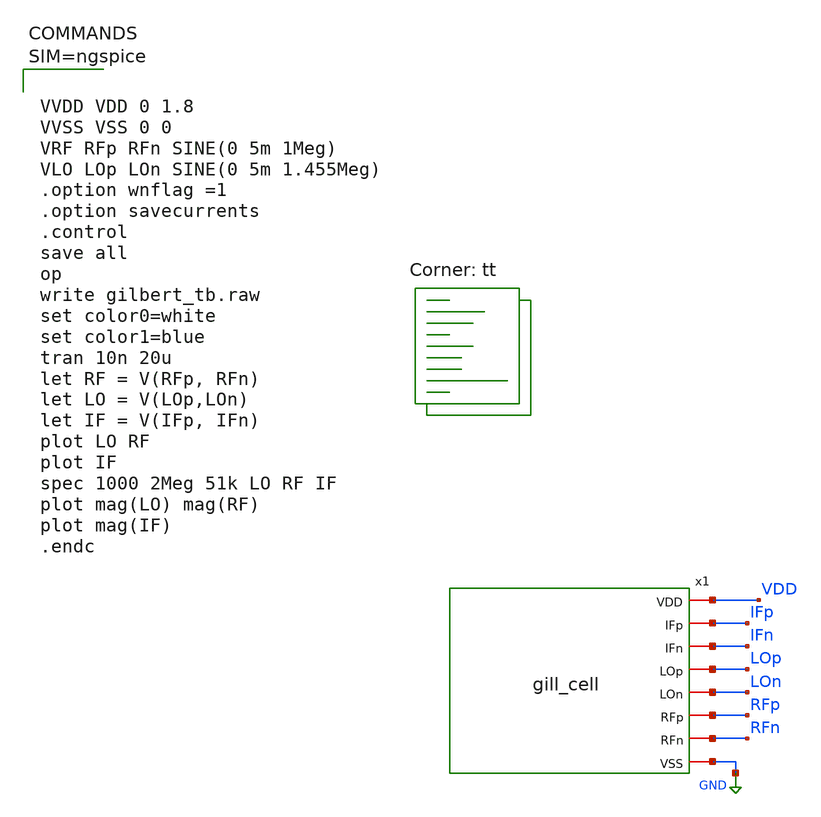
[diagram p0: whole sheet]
** sch_path: hw03/xschem/gilbert_tb.sch
**.subckt gilbert_tb
x1 VDD IFp IFn LOp LOn RFp RFn GND gill_cell
**** begin user architecture code



VVDD VDD 0 1.8
VVSS VSS 0 0
VRF RFp RFn SINE(0 5m 1Meg)
VLO LOp LOn SINE(0 5m 1.455Meg)
.option wnflag =1
.option savecurrents
.control
save all
op
write gilbert_tb.raw
set color0=white
set color1=blue
tran 10n 20u
let RF = V(RFp, RFn)
let LO = V(LOp,LOn)
let IF = V(IFp, IFn)
plot LO RF
plot IF
spec 1000 2Meg 51k LO RF IF
plot mag(LO) mag(RF)
plot mag(IF)
.endc



.lib $::SKYWATER_MODELS/sky130.lib.spice tt
**** end user architecture code
**.ends

* expanding   symbol:  gill_cell.sym # of pins=8
** sym_path: hw03/xschem/gill_cell.sym
** sch_path: hw03/xschem/gill_cell.sch
.subckt gill_cell VDD IFp IFn LOp LOn RFp RFn VSS
*.ipin VSS
*.ipin VDD
*.iopin IFp
*.iopin IFn
*.iopin LOp
*.iopin LOn
*.iopin RFp
*.iopin RFn
XR1 IF++ VDD VSS sky130_fd_pr__res_xhigh_po_0p69 L=0.69*10 mult=1 m=1
XR3 IF-- VDD VSS sky130_fd_pr__res_xhigh_po_0p69 L=0.69*10 mult=1 m=1
XR2 VM VDD VSS sky130_fd_pr__res_xhigh_po_0p69 L=0.69*4.5 mult=1 m=1
XR4 VDD LOp VSS sky130_fd_pr__res_xhigh_po_0p69 L=0.69*2 mult=1 m=1
XR5 LOp VSS VSS sky130_fd_pr__res_xhigh_po_0p69 L=0.69*5 mult=1 m=1
XR10 VDD LOp VSS sky130_fd_pr__res_xhigh_po_0p69 L=0.69*2 mult=1 m=1
XR11 LOp VSS VSS sky130_fd_pr__res_xhigh_po_0p69 L=0.69*5 mult=1 m=1
XR6 VDD RFn VSS sky130_fd_pr__res_xhigh_po_0p69 L=0.69*5 mult=1 m=1
XR7 RFn VSS VSS sky130_fd_pr__res_xhigh_po_0p69 L=0.69*5 mult=1 m=1
XR8 VDD RFp VSS sky130_fd_pr__res_xhigh_po_0p69 L=0.69*5 mult=1 m=1
XR9 RFp VSS VSS sky130_fd_pr__res_xhigh_po_0p69 L=0.69*5 mult=1 m=1
XR12 LOn VDD VSS sky130_fd_pr__res_xhigh_po_0p69 L=0.69*2 mult=1 m=1
XR13 VSS LOn VSS sky130_fd_pr__res_xhigh_po_0p69 L=0.69*5 mult=1 m=1
XM2 net5 VM VSS VSS sky130_fd_pr__nfet_01v8 L=1 W=40 nf=1 ad='int((nf+1)/2) * W/nf * 0.29' as='int((nf+2)/2) * W/nf * 0.29'
+ pd='2*int((nf+1)/2) * (W/nf + 0.29)' ps='2*int((nf+2)/2) * (W/nf + 0.29)' nrd='0.29 / W' nrs='0.29 / W'
+ sa=0 sb=0 sd=0 mult=1 m=1
XM3 net2 RFp net1 VSS sky130_fd_pr__nfet_01v8 L=1 W=40 nf=1 ad='int((nf+1)/2) * W/nf * 0.29' as='int((nf+2)/2) * W/nf * 0.29'
+ pd='2*int((nf+1)/2) * (W/nf + 0.29)' ps='2*int((nf+2)/2) * (W/nf + 0.29)' nrd='0.29 / W' nrs='0.29 / W'
+ sa=0 sb=0 sd=0 mult=1 m=1
XM5 IF++ LOp net2 VSS sky130_fd_pr__nfet_01v8 L=1 W=40 nf=1 ad='int((nf+1)/2) * W/nf * 0.29' as='int((nf+2)/2) * W/nf * 0.29'
+ pd='2*int((nf+1)/2) * (W/nf + 0.29)' ps='2*int((nf+2)/2) * (W/nf + 0.29)' nrd='0.29 / W' nrs='0.29 / W'
+ sa=0 sb=0 sd=0 mult=1 m=1
XM7 IF++ LOn net3 VSS sky130_fd_pr__nfet_01v8 L=1 W=40 nf=1 ad='int((nf+1)/2) * W/nf * 0.29' as='int((nf+2)/2) * W/nf * 0.29'
+ pd='2*int((nf+1)/2) * (W/nf + 0.29)' ps='2*int((nf+2)/2) * (W/nf + 0.29)' nrd='0.29 / W' nrs='0.29 / W'
+ sa=0 sb=0 sd=0 mult=1 m=1
XM1 VM VM VSS VSS sky130_fd_pr__nfet_01v8 L=1 W=40 nf=1 ad='int((nf+1)/2) * W/nf * 0.29' as='int((nf+2)/2) * W/nf * 0.29'
+ pd='2*int((nf+1)/2) * (W/nf + 0.29)' ps='2*int((nf+2)/2) * (W/nf + 0.29)' nrd='0.29 / W' nrs='0.29 / W'
+ sa=0 sb=0 sd=0 mult=1 m=1
XM4 net3 RFn net1 VSS sky130_fd_pr__nfet_01v8 L=1 W=40 nf=1 ad='int((nf+1)/2) * W/nf * 0.29' as='int((nf+2)/2) * W/nf * 0.29'
+ pd='2*int((nf+1)/2) * (W/nf + 0.29)' ps='2*int((nf+2)/2) * (W/nf + 0.29)' nrd='0.29 / W' nrs='0.29 / W'
+ sa=0 sb=0 sd=0 mult=1 m=1
XM8 IF-- LOp net3 VSS sky130_fd_pr__nfet_01v8 L=1 W=40 nf=1 ad='int((nf+1)/2) * W/nf * 0.29' as='int((nf+2)/2) * W/nf * 0.29'
+ pd='2*int((nf+1)/2) * (W/nf + 0.29)' ps='2*int((nf+2)/2) * (W/nf + 0.29)' nrd='0.29 / W' nrs='0.29 / W'
+ sa=0 sb=0 sd=0 mult=1 m=1
XM6 IF-- LOn net2 VSS sky130_fd_pr__nfet_01v8 L=1 W=40 nf=1 ad='int((nf+1)/2) * W/nf * 0.29' as='int((nf+2)/2) * W/nf * 0.29'
+ pd='2*int((nf+1)/2) * (W/nf + 0.29)' ps='2*int((nf+2)/2) * (W/nf + 0.29)' nrd='0.29 / W' nrs='0.29 / W'
+ sa=0 sb=0 sd=0 mult=1 m=1
XM9 net4 VM VSS VSS sky130_fd_pr__nfet_01v8 L=1 W=40 nf=1 ad='int((nf+1)/2) * W/nf * 0.29' as='int((nf+2)/2) * W/nf * 0.29'
+ pd='2*int((nf+1)/2) * (W/nf + 0.29)' ps='2*int((nf+2)/2) * (W/nf + 0.29)' nrd='0.29 / W' nrs='0.29 / W'
+ sa=0 sb=0 sd=0 mult=1 m=1
XM10 IFn IF-- net4 VSS sky130_fd_pr__nfet_01v8 L=1 W=40 nf=1 ad='int((nf+1)/2) * W/nf * 0.29' as='int((nf+2)/2) * W/nf * 0.29'
+ pd='2*int((nf+1)/2) * (W/nf + 0.29)' ps='2*int((nf+2)/2) * (W/nf + 0.29)' nrd='0.29 / W' nrs='0.29 / W'
+ sa=0 sb=0 sd=0 mult=1 m=1
XM11 IFp IF++ net4 VSS sky130_fd_pr__nfet_01v8 L=1 W=40 nf=1 ad='int((nf+1)/2) * W/nf * 0.29' as='int((nf+2)/2) * W/nf * 0.29'
+ pd='2*int((nf+1)/2) * (W/nf + 0.29)' ps='2*int((nf+2)/2) * (W/nf + 0.29)' nrd='0.29 / W' nrs='0.29 / W'
+ sa=0 sb=0 sd=0 mult=1 m=1
XR14 IFp VDD VSS sky130_fd_pr__res_xhigh_po_0p69 L=0.69*14 mult=1 m=1
XR15 IFn VDD VSS sky130_fd_pr__res_xhigh_po_0p69 L=0.69*14 mult=1 m=1
**** begin user architecture code



VVDD VDD 0 1.8
VVSS VSS 0 0
VRF RFp RFn SINE(0 5m 1k)
VLO LOp LOn SINE(0 5m 1.1k)
.control
save all
set color0=white
set color1=blue
tran 10u 20m
write gilbert_tb.raw
let RF = V(RFp, RFn)
let LO = V(LOp,LOn)
let IF = V(IFp, IFn)
plot LO RF
plot IF
spec 10 3k 100 LO RF IF
plot mag(LO) mag(RF)
plot mag(IF)
.endc



**** end user architecture code
Vmeas net1 net5 0
.save i(vmeas)
.ends

.GLOBAL GND
.end
